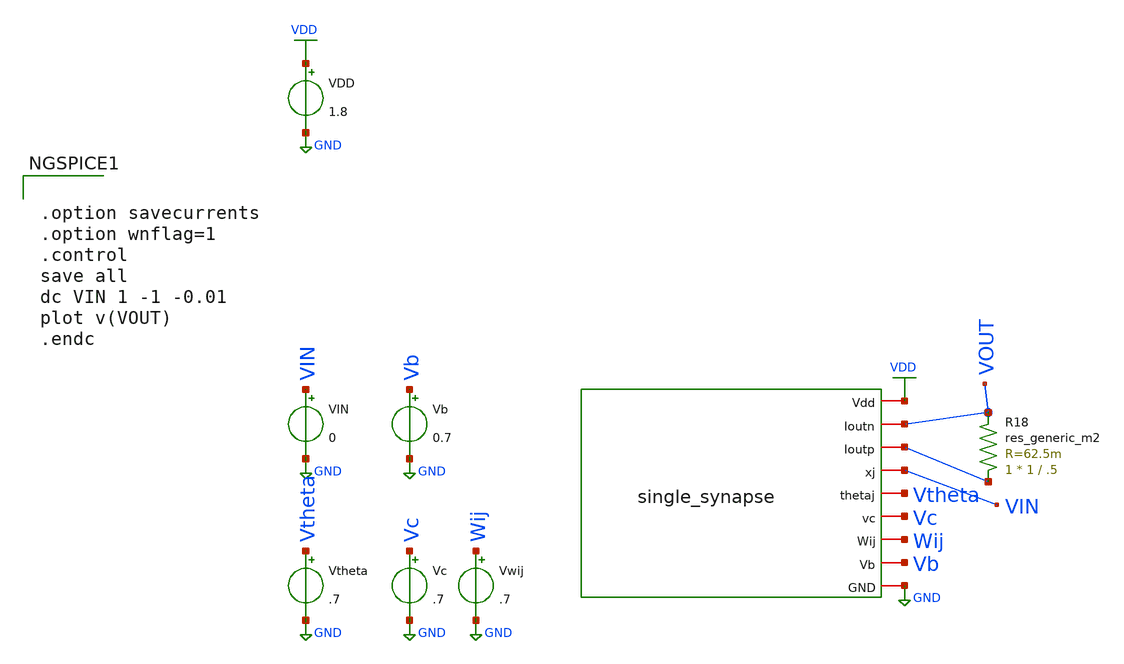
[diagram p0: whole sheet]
** sch_path: test_single_synapse.sch
**.subckt test_single_synapse
x1 VDD VOUT net1 VIN Vtheta Vc Wij Vb GND single_synapse
VDD VDD GND 1.8
VIN VIN GND 0
R18 net1 VOUT sky130_fd_pr__res_generic_m2 W=1 L=.5 m=1
Vb Vb GND 0.7
Vtheta Vtheta GND .7
Vc Vc GND .7
Vwij Wij GND .7
**** begin user architecture code


.option savecurrents
.option wnflag=1
.control
save all
dc VIN 1 -1 -0.01
plot v(VOUT)
.endc



** opencircuitdesign pdks install
.lib $::SKYWATER_MODELS/sky130.lib.spice tt


**** end user architecture code
**.ends
.GLOBAL GND
.GLOBAL VDD
.end
